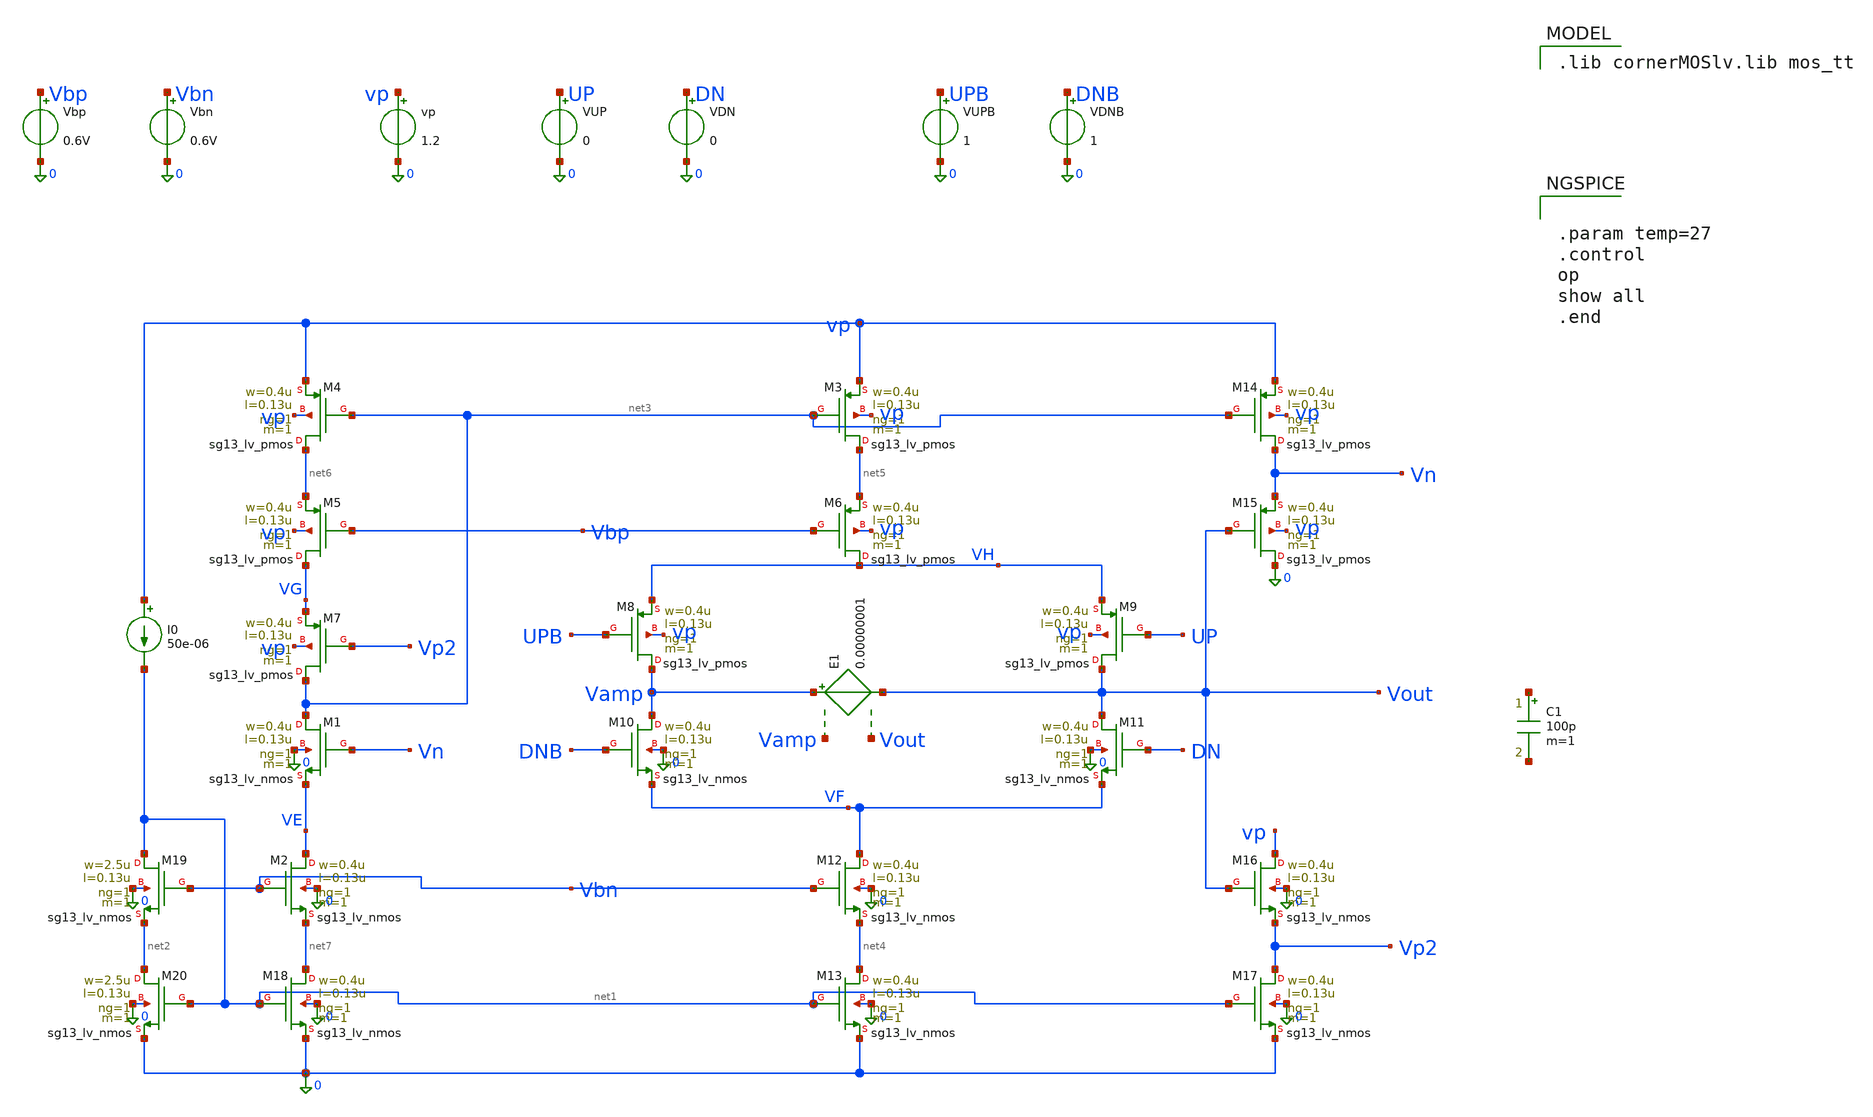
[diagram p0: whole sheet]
** sch_path: charge_pump/cp_v3_tb (4).sch
**.subckt cp_v3_tb (4)
C1 net8 net9 100p m=1
vp vp 0 1.2
VUP UP 0 0
VDN DN 0 0
Vbp Vbp 0 0.6V
Vbn Vbn 0 0.6V
VUPB UPB 0 1
VDNB DNB 0 1
XM1 net3 Vn VE 0 sg13_lv_nmos w=0.4u l=0.13u ng=1 m=1 mm_ok=1
XM3 net5 net3 vp vp sg13_lv_pmos w=0.4u l=0.13u ng=1 m=1 mm_ok=1
XM4 net6 net3 vp vp sg13_lv_pmos w=0.4u l=0.13u ng=1 m=1 mm_ok=1
XM5 VG Vbp net6 vp sg13_lv_pmos w=0.4u l=0.13u ng=1 m=1 mm_ok=1
XM6 VH Vbp net5 vp sg13_lv_pmos w=0.4u l=0.13u ng=1 m=1 mm_ok=1
XM7 net3 Vp2 VG vp sg13_lv_pmos w=0.4u l=0.13u ng=1 m=1 mm_ok=1
XM8 Vamp UPB VH vp sg13_lv_pmos w=0.4u l=0.13u ng=1 m=1 mm_ok=1
XM9 Vout UP VH vp sg13_lv_pmos w=0.4u l=0.13u ng=1 m=1 mm_ok=1
XM10 Vamp DNB VF 0 sg13_lv_nmos w=0.4u l=0.13u ng=1 m=1 mm_ok=1
XM11 Vout DN VF 0 sg13_lv_nmos w=0.4u l=0.13u ng=1 m=1 mm_ok=1
XM12 VF Vbn net4 0 sg13_lv_nmos w=0.4u l=0.13u ng=1 m=1 mm_ok=1
XM13 net4 net1 0 0 sg13_lv_nmos w=0.4u l=0.13u ng=1 m=1 mm_ok=1
XM14 Vn net3 vp vp sg13_lv_pmos w=0.4u l=0.13u ng=1 m=1 mm_ok=1
XM15 0 Vout Vn vp sg13_lv_pmos w=0.4u l=0.13u ng=1 m=1 mm_ok=1
XM16 vp Vout Vp2 0 sg13_lv_nmos w=0.4u l=0.13u ng=1 m=1 mm_ok=1
XM17 Vp2 net1 0 0 sg13_lv_nmos w=0.4u l=0.13u ng=1 m=1 mm_ok=1
XM2 VE Vbn net7 0 sg13_lv_nmos w=0.4u l=0.13u ng=1 m=1 mm_ok=1
XM18 net7 net1 0 0 sg13_lv_nmos w=0.4u l=0.13u ng=1 m=1 mm_ok=1
XM19 net1 Vbn net2 0 sg13_lv_nmos w=2.5u l=0.13u ng=1 m=1 mm_ok=1
XM20 net2 net1 0 0 sg13_lv_nmos w=2.5u l=0.13u ng=1 m=1 mm_ok=1
I0 vp net1 50e-06
E1 Vamp Vout Vamp Vout 0.00000001
**** begin user architecture code
 .lib cornerMOSlv.lib mos_tt



.param temp=27
.control
op
show all
.end


**** end user architecture code
**.ends
.end
